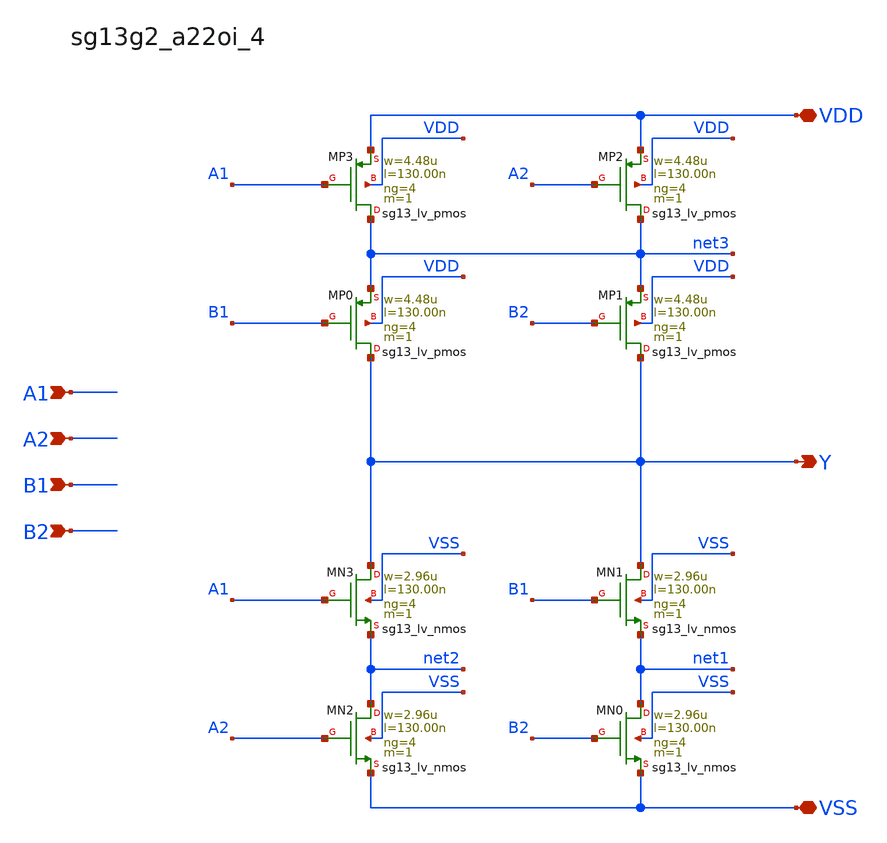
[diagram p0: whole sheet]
** sch_path: outputs/sg13g2_cells/cells/sg13g2_a22oi_4/sg13g2_a22oi_4.sch
**.subckt sg13g2_a22oi_4 Y A1 A2 B1 B2 VDD VSS
*.opin Y
*.ipin A1
*.ipin A2
*.ipin B1
*.ipin B2
*.iopin VDD
*.iopin VSS
XMN0 net1 B2 VSS VSS sg13_lv_nmos w=2.96u l=130.00n ng=4 m=1 mm_ok=1
XMN1 Y B1 net1 VSS sg13_lv_nmos w=2.96u l=130.00n ng=4 m=1 mm_ok=1
XMN2 net2 A2 VSS VSS sg13_lv_nmos w=2.96u l=130.00n ng=4 m=1 mm_ok=1
XMN3 Y A1 net2 VSS sg13_lv_nmos w=2.96u l=130.00n ng=4 m=1 mm_ok=1
XMP0 Y B1 net3 VDD sg13_lv_pmos w=4.48u l=130.00n ng=4 m=1 mm_ok=1
XMP1 Y B2 net3 VDD sg13_lv_pmos w=4.48u l=130.00n ng=4 m=1 mm_ok=1
XMP2 net3 A2 VDD VDD sg13_lv_pmos w=4.48u l=130.00n ng=4 m=1 mm_ok=1
XMP3 net3 A1 VDD VDD sg13_lv_pmos w=4.48u l=130.00n ng=4 m=1 mm_ok=1
**.ends
.end
